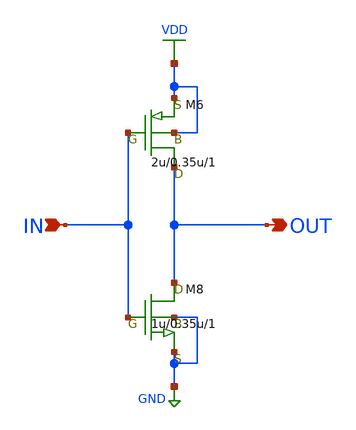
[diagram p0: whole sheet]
** sch_path: LR_hasegawa/LR_Work2/symbol/INVERTER.sch
**.subckt INVERTER OUT IN
*.opin OUT
*.ipin IN
M6 OUT IN VDD VDD pch w=2u l=0.35u as=5.6p ps=9u ad=5.6p pd=9u m=1
M8 OUT IN GND GND nch w=1u l=0.35u as=2.8p ps=5.5u ad=2.8p pd=5.5u m=1
**.ends
.GLOBAL VDD
.GLOBAL GND
.end
